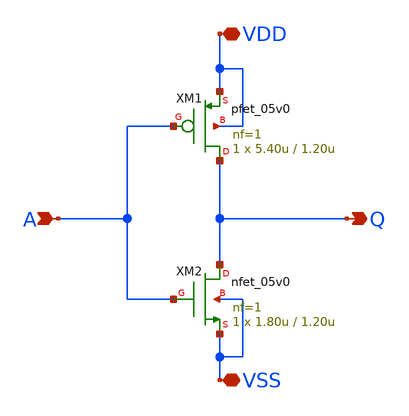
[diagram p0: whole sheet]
** sch_path: inv_dut_108.sch
**.subckt inv_dut_108 VDD VSS A Q
*.iopin VDD
*.iopin VSS
*.ipin A
*.opin Q
XM1 Q A VDD VDD pfet_05v0 L=1.20u W=5.40u nf=1 ad='int((nf+1)/2) * W/nf * 0.18u' as='int((nf+2)/2) * W/nf * 0.18u'
+ pd='2*int((nf+1)/2) * (W/nf + 0.18u)' ps='2*int((nf+2)/2) * (W/nf + 0.18u)' nrd='0.18u / W' nrs='0.18u / W'
+ sa=0 sb=0 sd=0 m=1
XM2 Q A VSS VSS nfet_05v0 L=1.20u W=1.80u nf=1 ad='int((nf+1)/2) * W/nf * 0.18u' as='int((nf+2)/2) * W/nf * 0.18u'
+ pd='2*int((nf+1)/2) * (W/nf + 0.18u)' ps='2*int((nf+2)/2) * (W/nf + 0.18u)' nrd='0.18u / W' nrs='0.18u / W'
+ sa=0 sb=0 sd=0 m=1
**.ends
.end
